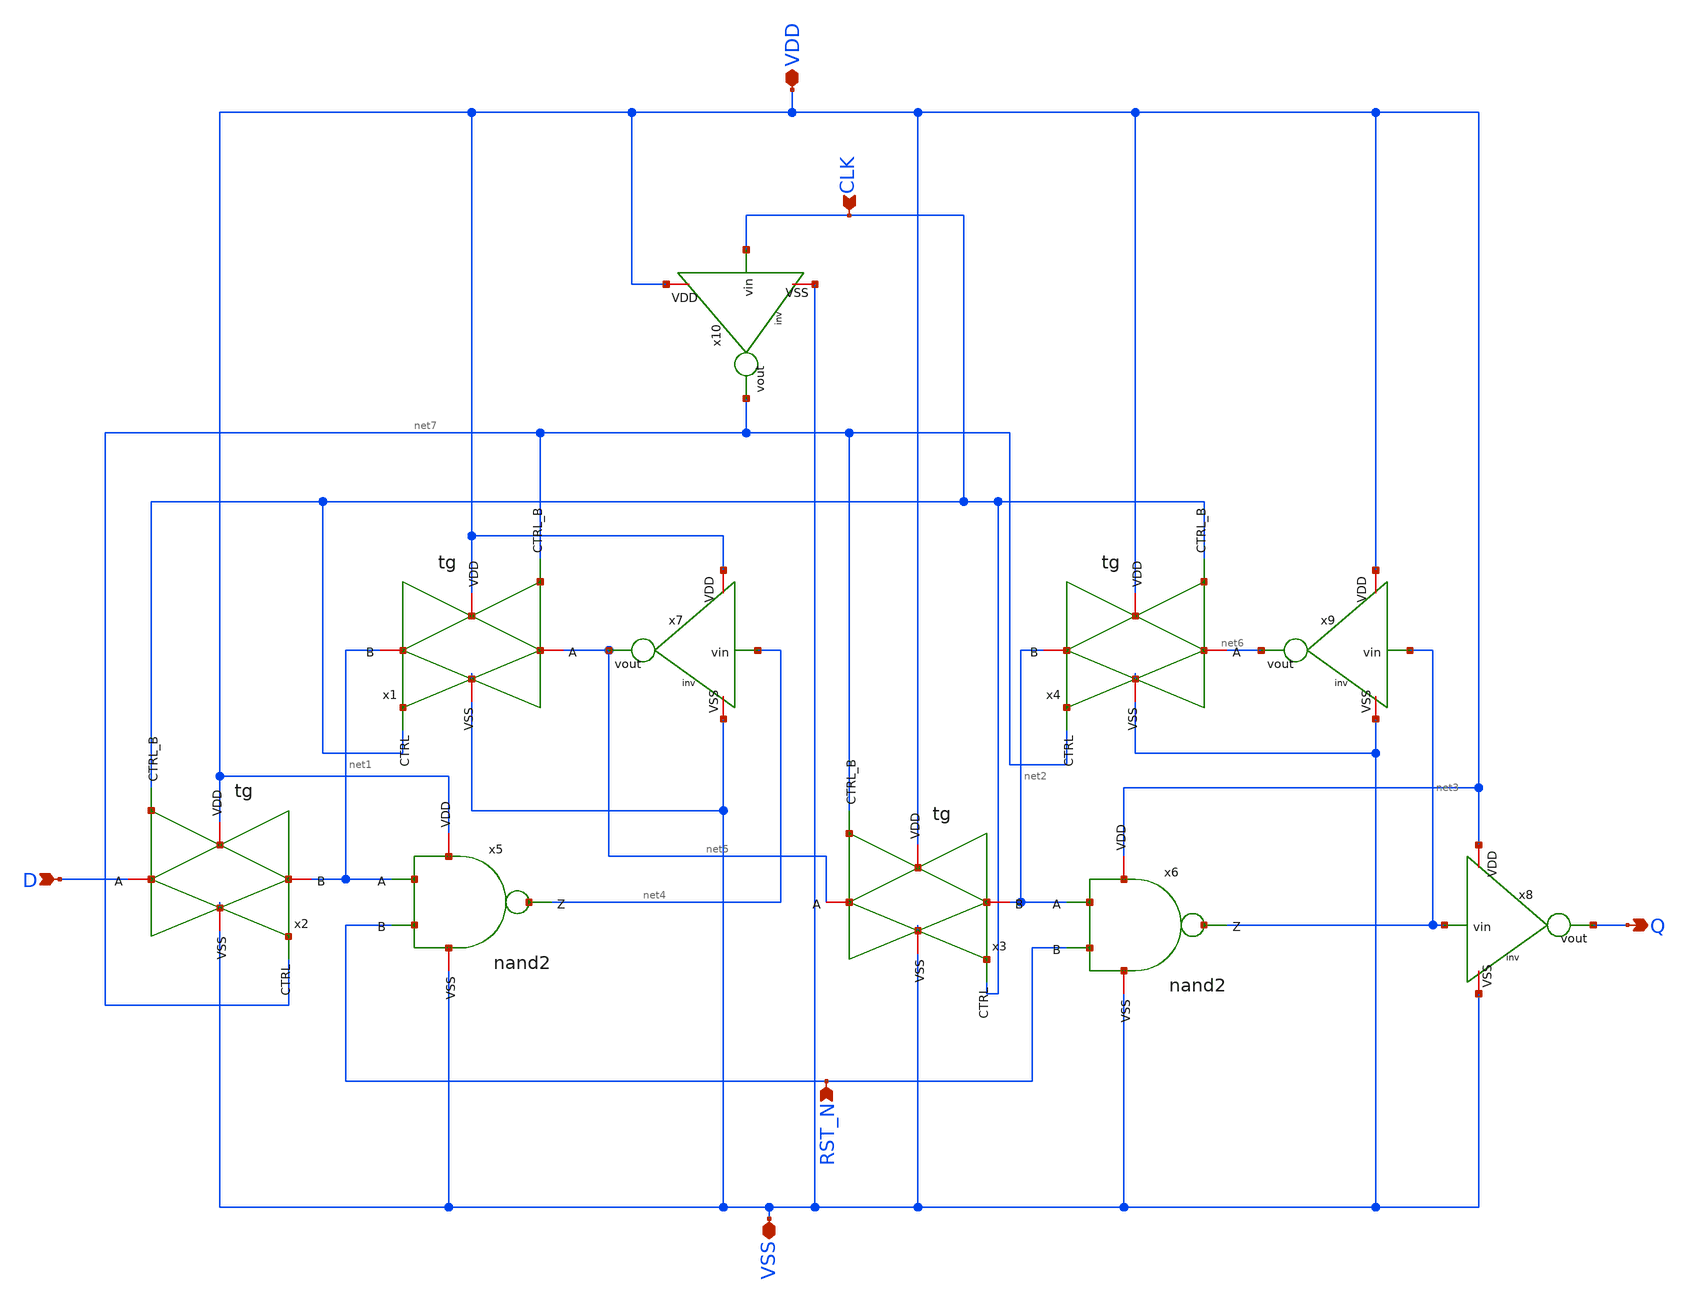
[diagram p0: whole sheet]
** sch_path: sar_logic/sar_designs/dff_rst_n.sch
**.subckt dff_rst_n D CLK RST_N Q VDD VSS
*.ipin D
*.ipin CLK
*.ipin RST_N
*.opin Q
*.iopin VDD
*.iopin VSS
x1 CLK VSS net5 net1 VDD net7 tg
x2 net7 VSS D net1 VDD CLK tg
x3 CLK VSS net5 net2 VDD net7 tg
x4 net7 VSS net6 net2 VDD CLK tg
x5 VDD net4 net1 RST_N VSS nand2
x6 VDD net3 net2 RST_N VSS nand2
x7 VDD net4 net5 VSS inv
x8 VDD net3 Q VSS inv
x9 VDD net3 net6 VSS inv
x10 VDD CLK net7 VSS inv
**.ends

* expanding   symbol:  tg.sym # of pins=6
** sym_path: sar_logic/sar_designs/tg.sym
** sch_path: sar_logic/sar_designs/tg.sch
.subckt tg CTRL VSS A B VDD CTRL_B
*.iopin VDD
*.iopin VSS
*.iopin A
*.iopin B
*.ipin CTRL_B
*.ipin CTRL
XM1 A CTRL_B B VDD pfet_03v3 L=0.28u W=1u nf=1 ad='int((nf+1)/2) * W/nf * 0.18u' as='int((nf+2)/2) * W/nf * 0.18u'
+ pd='2*int((nf+1)/2) * (W/nf + 0.18u)' ps='2*int((nf+2)/2) * (W/nf + 0.18u)' nrd='0.18u / W' nrs='0.18u / W'
+ sa=0 sb=0 sd=0 m=1
XM2 A CTRL B VSS nfet_03v3 L=0.28u W=0.5u nf=1 ad='int((nf+1)/2) * W/nf * 0.18u' as='int((nf+2)/2) * W/nf * 0.18u'
+ pd='2*int((nf+1)/2) * (W/nf + 0.18u)' ps='2*int((nf+2)/2) * (W/nf + 0.18u)' nrd='0.18u / W' nrs='0.18u / W'
+ sa=0 sb=0 sd=0 m=1
.ends


* expanding   symbol:  nand2.sym # of pins=5
** sym_path: sar_logic/sar_designs/nand2.sym
** sch_path: sar_logic/sar_designs/nand2.sch
.subckt nand2 VDD Z A B VSS
*.ipin A
*.ipin B
*.iopin VSS
*.iopin VDD
*.opin Z
XM1 Z A VDD VDD pfet_03v3 L=0.28u W=1u nf=1 ad='int((nf+1)/2) * W/nf * 0.18u' as='int((nf+2)/2) * W/nf * 0.18u'
+ pd='2*int((nf+1)/2) * (W/nf + 0.18u)' ps='2*int((nf+2)/2) * (W/nf + 0.18u)' nrd='0.18u / W' nrs='0.18u / W'
+ sa=0 sb=0 sd=0 m=1
XM2 Z B VDD VDD pfet_03v3 L=0.28u W=1u nf=1 ad='int((nf+1)/2) * W/nf * 0.18u' as='int((nf+2)/2) * W/nf * 0.18u'
+ pd='2*int((nf+1)/2) * (W/nf + 0.18u)' ps='2*int((nf+2)/2) * (W/nf + 0.18u)' nrd='0.18u / W' nrs='0.18u / W'
+ sa=0 sb=0 sd=0 m=1
XM3 Z A net1 VSS nfet_03v3 L=0.28u W=1u nf=1 ad='int((nf+1)/2) * W/nf * 0.18u' as='int((nf+2)/2) * W/nf * 0.18u'
+ pd='2*int((nf+1)/2) * (W/nf + 0.18u)' ps='2*int((nf+2)/2) * (W/nf + 0.18u)' nrd='0.18u / W' nrs='0.18u / W'
+ sa=0 sb=0 sd=0 m=1
XM4 net1 B VSS VSS nfet_03v3 L=0.28u W=1u nf=1 ad='int((nf+1)/2) * W/nf * 0.18u' as='int((nf+2)/2) * W/nf * 0.18u'
+ pd='2*int((nf+1)/2) * (W/nf + 0.18u)' ps='2*int((nf+2)/2) * (W/nf + 0.18u)' nrd='0.18u / W' nrs='0.18u / W'
+ sa=0 sb=0 sd=0 m=1
.ends


* expanding   symbol:  inv.sym # of pins=4
** sym_path: sar_logic/sar_designs/inv.sym
** sch_path: sar_logic/sar_designs/inv.sch
.subckt inv VDD vin vout VSS
*.ipin vin
*.opin vout
*.iopin VDD
*.iopin VSS
XM1 vout vin VDD VDD pfet_03v3 L=0.28u W=1u nf=1 ad='int((nf+1)/2) * W/nf * 0.18u' as='int((nf+2)/2) * W/nf * 0.18u'
+ pd='2*int((nf+1)/2) * (W/nf + 0.18u)' ps='2*int((nf+2)/2) * (W/nf + 0.18u)' nrd='0.18u / W' nrs='0.18u / W'
+ sa=0 sb=0 sd=0 m=1
XM2 vout vin VSS VSS nfet_03v3 L=0.28u W=0.5u nf=1 ad='int((nf+1)/2) * W/nf * 0.18u' as='int((nf+2)/2) * W/nf * 0.18u'
+ pd='2*int((nf+1)/2) * (W/nf + 0.18u)' ps='2*int((nf+2)/2) * (W/nf + 0.18u)' nrd='0.18u / W' nrs='0.18u / W'
+ sa=0 sb=0 sd=0 m=1
.ends

.end
